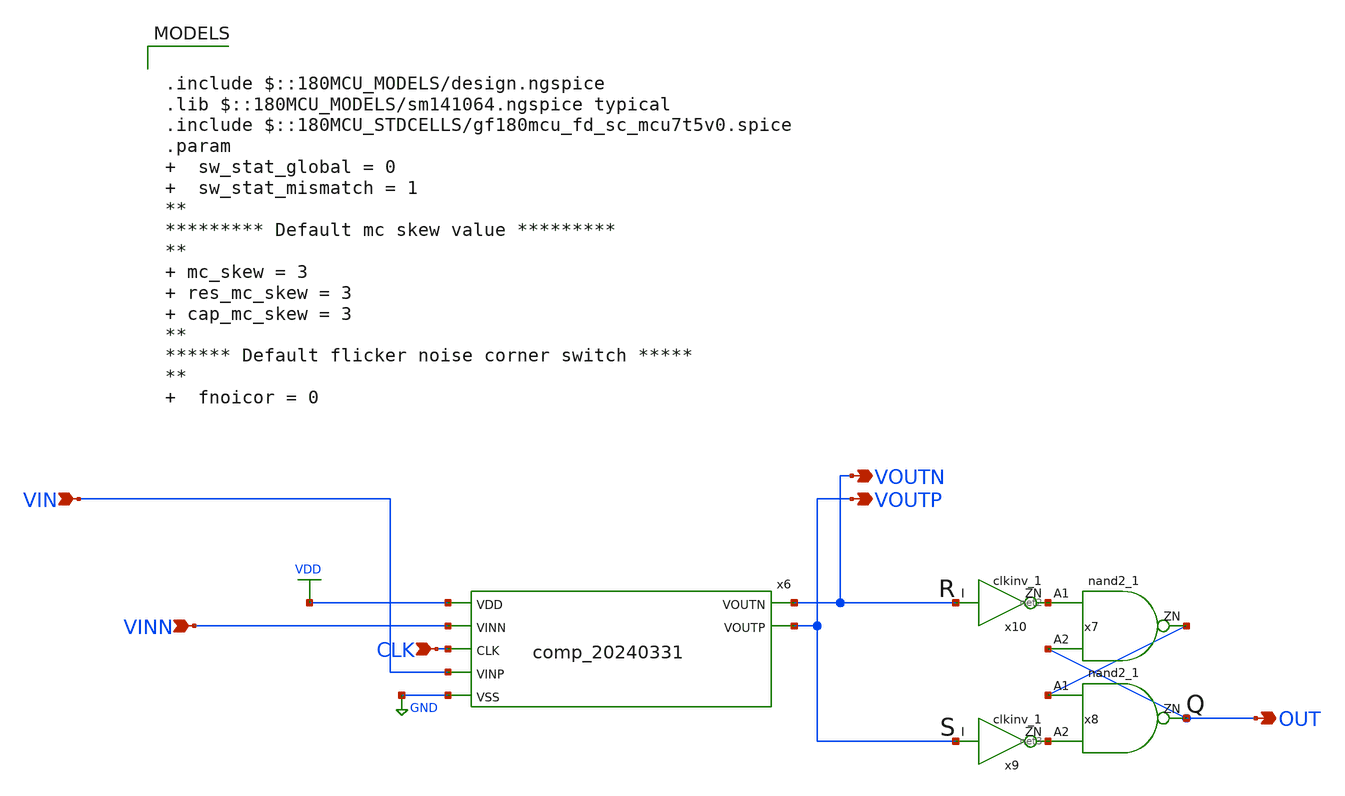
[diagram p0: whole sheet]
** sch_path: gitefu/tb/tb_like_p81.sch
**.subckt tb_like_p81 VIN VINN CLK VOUTN VOUTP OUT
*.ipin VIN
*.ipin VINN
*.ipin CLK
*.opin VOUTN
*.opin VOUTP
*.opin OUT
x6 VDD CLK VOUTP VOUTN VIN VINN GND TOP
x7 net2 OUT net1 VDD VDD 0 0 gf180mcu_fd_sc_mcu7t5v0__nand2_1
x8 net1 net3 OUT VDD VDD 0 0 gf180mcu_fd_sc_mcu7t5v0__nand2_1
x9 VOUTP net3 VDD VDD 0 0 gf180mcu_fd_sc_mcu7t5v0__clkinv_1
x10 VOUTN net2 VDD VDD 0 0 gf180mcu_fd_sc_mcu7t5v0__clkinv_1
**** begin user architecture code



.include /media/tomoakitanaka/Documents/MyDocuments/personal/ISHIKAI/2024/Chipathon2023_ADC/gitefu/comp_20240331/TOP_pex_extracted.spice
VPW VDD 0 dc 3.3
VCL CLK 0 pulse (0 3.3 0 40p 40p 62.5n 125n) dc 0
VIN VIN 0 pwl(0 0 0.01m 3.3) dc 0
VCO VINN 0 pwl(0 3.3 0.01m 0) dc 0
.control
set wr_vecnames
set wr_singlescale
let count=0
dowhile count < 10
  save VINN VIN OUT
  tran 10n 0.01m
  write VOUT_EXT.raw
  set appendwrite
  reset
  let count = count + 1
end
.endc




.include $::180MCU_MODELS/design.ngspice
.lib $::180MCU_MODELS/sm141064.ngspice typical
.include $::180MCU_STDCELLS/gf180mcu_fd_sc_mcu7t5v0.spice
.param   sw_stat_global = 0   sw_stat_mismatch = 1
**
********* Default mc skew value *********
**  mc_skew = 3  res_mc_skew = 3  cap_mc_skew = 3
**
****** Default flicker noise corner switch *****
**   fnoicor = 0

**** end user architecture code
**.ends
.GLOBAL GND
.GLOBAL VDD
.end
